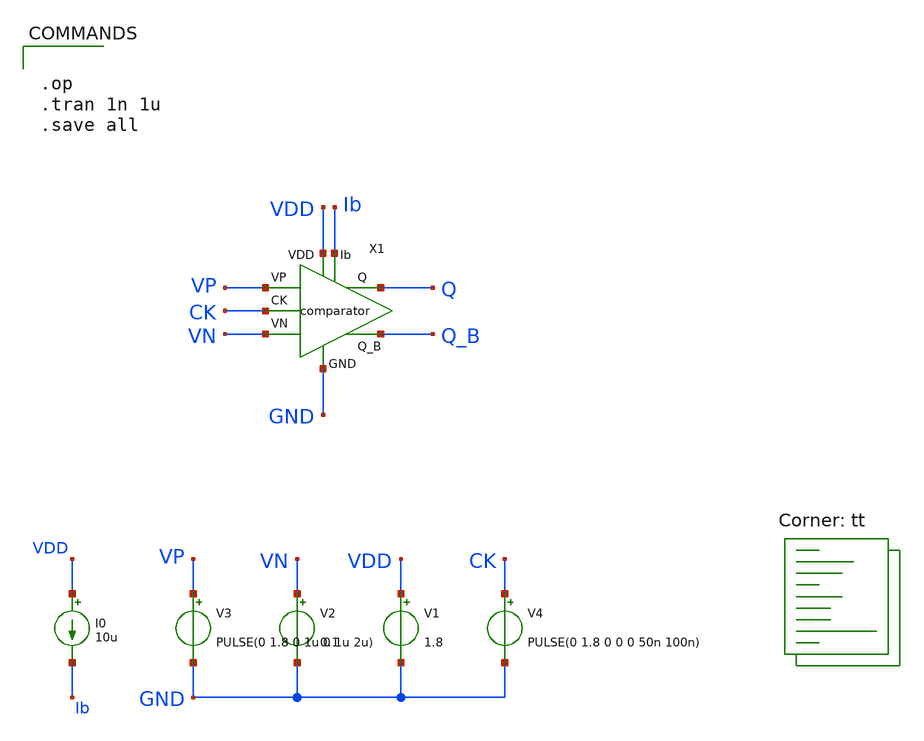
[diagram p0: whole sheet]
** sch_path: xschem/comparator/comparator_tb.sch
**.subckt comparator_tb
V1 VDD GND 1.8
V2 VN GND 0.1
V3 VP GND PULSE(0 1.8 0 1u 0 1u 2u)
V4 CK GND PULSE(0 1.8 0 0 0 50n 100n)
X1 VP VN GND Q_B Q VDD CK Ib comparator
I0 VDD Ib 10u
**** begin user architecture code
.lib $::SKYWATER_MODELS/sky130.lib.spice tt


.op
.tran 1n 1u
.save all


**** end user architecture code
**.ends
.end
